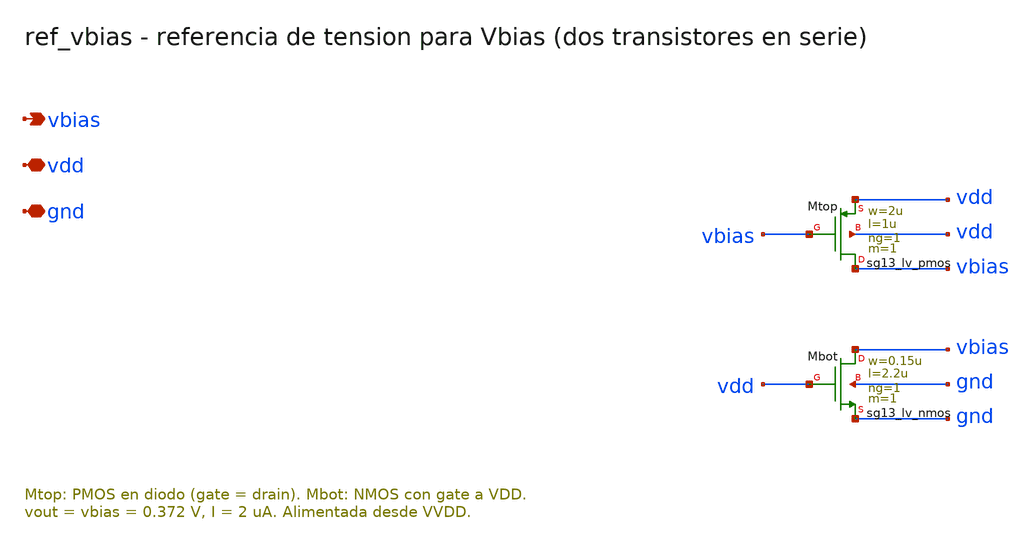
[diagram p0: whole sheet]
** sch_path: Enfoque_B/xschem/celdas/ref_vbias.sch
**.subckt ref_vbias vbias vdd gnd
*.opin vbias
*.iopin vdd
*.iopin gnd
XMtop vbias vbias vdd vdd sg13_lv_pmos w=2u l=1u ng=1 m=1 mm_ok=1
XMbot vbias vdd gnd gnd sg13_lv_nmos w=0.15u l=2.2u ng=1 m=1 mm_ok=1
**.ends
.end
